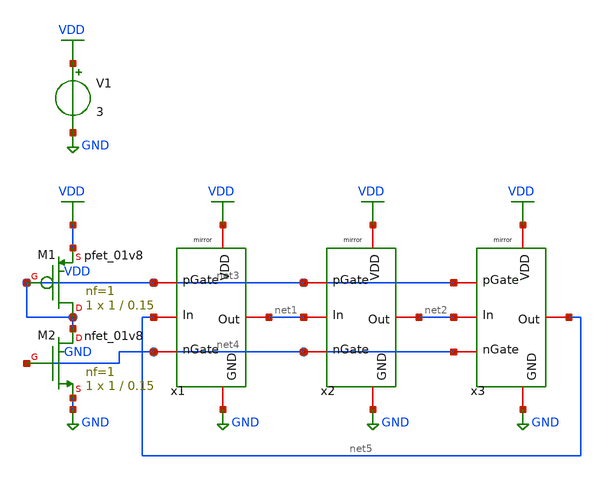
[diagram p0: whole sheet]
** sch_path: VCO_circuit/VCO_tb.sch
**.subckt VCO_tb
x1 VDD net3 net5 net1 net4 GND current_mirror
x2 VDD net3 net1 net2 net4 GND current_mirror
x3 VDD net3 net2 net5 net4 GND current_mirror
XM1 net3 net3 VDD VDD sky130_fd_pr__pfet_01v8 L=0.15 W=1 nf=1 ad='int((nf+1)/2) * W/nf * 0.29' as='int((nf+2)/2) * W/nf * 0.29'
+ pd='2*int((nf+1)/2) * (W/nf + 0.29)' ps='2*int((nf+2)/2) * (W/nf + 0.29)' nrd='0.29 / W' nrs='0.29 / W'
+ sa=0 sb=0 sd=0 mult=1 m=1
XM2 net3 net4 GND GND sky130_fd_pr__nfet_01v8 L=0.15 W=1 nf=1 ad='int((nf+1)/2) * W/nf * 0.29' as='int((nf+2)/2) * W/nf * 0.29'
+ pd='2*int((nf+1)/2) * (W/nf + 0.29)' ps='2*int((nf+2)/2) * (W/nf + 0.29)' nrd='0.29 / W' nrs='0.29 / W'
+ sa=0 sb=0 sd=0 mult=1 m=1
V1 VDD GND 3
**.ends

* expanding   symbol:  /home/kandiasrw/project/VCO_circuit/current_mirror.sym # of pins=6
** sym_path: VCO_circuit/current_mirror.sym
** sch_path: VCO_circuit/current_mirror.sch
.subckt current_mirror VDD pGate In Out nGate GND
*.iopin Out
*.iopin In
*.iopin VDD
*.iopin GND
*.iopin pGate
*.iopin nGate
XM1 Out In net2 VDD sky130_fd_pr__pfet_01v8 L=0.15 W=1 nf=1 ad='int((nf+1)/2) * W/nf * 0.29' as='int((nf+2)/2) * W/nf * 0.29'
+ pd='2*int((nf+1)/2) * (W/nf + 0.29)' ps='2*int((nf+2)/2) * (W/nf + 0.29)' nrd='0.29 / W' nrs='0.29 / W'
+ sa=0 sb=0 sd=0 mult=1 m=1
XM2 Out In net1 GND sky130_fd_pr__nfet_01v8 L=0.15 W=1 nf=1 ad='int((nf+1)/2) * W/nf * 0.29' as='int((nf+2)/2) * W/nf * 0.29'
+ pd='2*int((nf+1)/2) * (W/nf + 0.29)' ps='2*int((nf+2)/2) * (W/nf + 0.29)' nrd='0.29 / W' nrs='0.29 / W'
+ sa=0 sb=0 sd=0 mult=1 m=1
XM3 net2 pGate VDD VDD sky130_fd_pr__pfet_01v8 L=0.15 W=1 nf=1 ad='int((nf+1)/2) * W/nf * 0.29' as='int((nf+2)/2) * W/nf * 0.29'
+ pd='2*int((nf+1)/2) * (W/nf + 0.29)' ps='2*int((nf+2)/2) * (W/nf + 0.29)' nrd='0.29 / W' nrs='0.29 / W'
+ sa=0 sb=0 sd=0 mult=1 m=1
XM4 net1 nGate GND GND sky130_fd_pr__nfet_01v8 L=0.15 W=1 nf=1 ad='int((nf+1)/2) * W/nf * 0.29' as='int((nf+2)/2) * W/nf * 0.29'
+ pd='2*int((nf+1)/2) * (W/nf + 0.29)' ps='2*int((nf+2)/2) * (W/nf + 0.29)' nrd='0.29 / W' nrs='0.29 / W'
+ sa=0 sb=0 sd=0 mult=1 m=1
.ends

.GLOBAL GND
.GLOBAL VDD
.end
